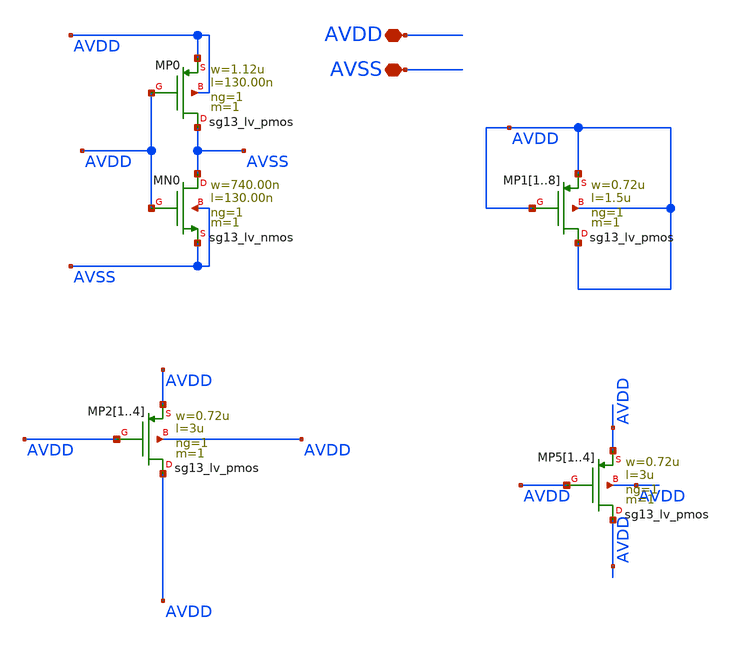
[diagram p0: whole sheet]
** sch_path: current_generator/analog/DAC/schematics/dac_DUMMIE.sch
**.subckt dac_DUMMIE AVDD AVSS
*.iopin AVDD
*.iopin AVSS
MMN0 AVSS AVDD AVSS AVSS sg13_lv_nmos w=740.00n l=130.00n ng=1 m=1 mm_ok=1
MMP0 AVSS AVDD AVDD AVDD sg13_lv_pmos w=1.12u l=130.00n ng=1 m=1 mm_ok=1
MMP11 AVDD AVDD AVDD AVDD sg13_lv_pmos w=0.72u l=1.5u ng=1 m=1 mm_ok=1
MMP12 AVDD AVDD AVDD AVDD sg13_lv_pmos w=0.72u l=1.5u ng=1 m=1 mm_ok=1
MMP13 AVDD AVDD AVDD AVDD sg13_lv_pmos w=0.72u l=1.5u ng=1 m=1 mm_ok=1
MMP14 AVDD AVDD AVDD AVDD sg13_lv_pmos w=0.72u l=1.5u ng=1 m=1 mm_ok=1
MMP15 AVDD AVDD AVDD AVDD sg13_lv_pmos w=0.72u l=1.5u ng=1 m=1 mm_ok=1
MMP16 AVDD AVDD AVDD AVDD sg13_lv_pmos w=0.72u l=1.5u ng=1 m=1 mm_ok=1
MMP17 AVDD AVDD AVDD AVDD sg13_lv_pmos w=0.72u l=1.5u ng=1 m=1 mm_ok=1
MMP18 AVDD AVDD AVDD AVDD sg13_lv_pmos w=0.72u l=1.5u ng=1 m=1 mm_ok=1
MMP51 AVDD AVDD AVDD AVDD sg13_lv_pmos w=0.72u l=3u ng=1 m=1 mm_ok=1
MMP52 AVDD AVDD AVDD AVDD sg13_lv_pmos w=0.72u l=3u ng=1 m=1 mm_ok=1
MMP53 AVDD AVDD AVDD AVDD sg13_lv_pmos w=0.72u l=3u ng=1 m=1 mm_ok=1
MMP54 AVDD AVDD AVDD AVDD sg13_lv_pmos w=0.72u l=3u ng=1 m=1 mm_ok=1
MMP21 AVDD AVDD AVDD AVDD sg13_lv_pmos w=0.72u l=3u ng=1 m=1 mm_ok=1
MMP22 AVDD AVDD AVDD AVDD sg13_lv_pmos w=0.72u l=3u ng=1 m=1 mm_ok=1
MMP23 AVDD AVDD AVDD AVDD sg13_lv_pmos w=0.72u l=3u ng=1 m=1 mm_ok=1
MMP24 AVDD AVDD AVDD AVDD sg13_lv_pmos w=0.72u l=3u ng=1 m=1 mm_ok=1
**.ends
.end
